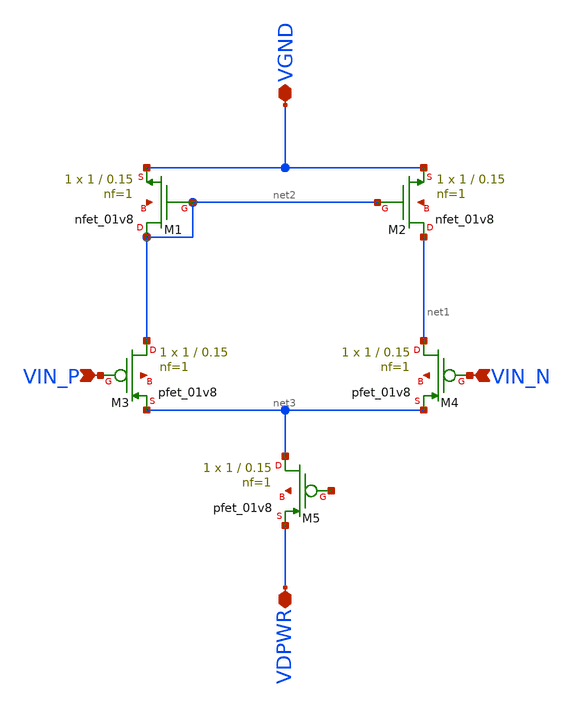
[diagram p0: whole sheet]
** sch_path: xschem/5t_ota.sch
**.subckt 5t_ota VGND VIN_N VIN_P VDPWR
*.iopin VGND
*.ipin VIN_N
*.ipin VIN_P
*.iopin VDPWR
XM1 net2 net2 VGND net4 sky130_fd_pr__nfet_01v8 L=0.15 W=1 nf=1 ad='int((1 + 1)/2) * 1 / 1 * 0.29' as='int((1 + 2)/2) * 1 / 1 * 0.29'
+ pd='2*int((1 + 1)/2) * (1 / 1 + 0.29)' ps='2*int((1 + 2)/2) * (1 / 1 + 0.29)' nrd='0.29 / 1 ' nrs='0.29 / 1 '
+ sa=0 sb=0 sd=0 mult=1 m=1
XM2 net1 net2 VGND net5 sky130_fd_pr__nfet_01v8 L=0.15 W=1 nf=1 ad='int((1 + 1)/2) * 1 / 1 * 0.29' as='int((1 + 2)/2) * 1 / 1 * 0.29'
+ pd='2*int((1 + 1)/2) * (1 / 1 + 0.29)' ps='2*int((1 + 2)/2) * (1 / 1 + 0.29)' nrd='0.29 / 1 ' nrs='0.29 / 1 '
+ sa=0 sb=0 sd=0 mult=1 m=1
XM3 net2 VIN_P net3 net6 sky130_fd_pr__pfet_01v8 L=0.15 W=1 nf=1 ad='int((1 + 1)/2) * 1 / 1 * 0.29' as='int((1 + 2)/2) * 1 / 1 * 0.29'
+ pd='2*int((1 + 1)/2) * (1 / 1 + 0.29)' ps='2*int((1 + 2)/2) * (1 / 1 + 0.29)' nrd='0.29 / 1 ' nrs='0.29 / 1 '
+ sa=0 sb=0 sd=0 mult=1 m=1
XM4 net1 VIN_N net3 net7 sky130_fd_pr__pfet_01v8 L=0.15 W=1 nf=1 ad='int((1 + 1)/2) * 1 / 1 * 0.29' as='int((1 + 2)/2) * 1 / 1 * 0.29'
+ pd='2*int((1 + 1)/2) * (1 / 1 + 0.29)' ps='2*int((1 + 2)/2) * (1 / 1 + 0.29)' nrd='0.29 / 1 ' nrs='0.29 / 1 '
+ sa=0 sb=0 sd=0 mult=1 m=1
XM5 net3 net8 VDPWR net9 sky130_fd_pr__pfet_01v8 L=0.15 W=1 nf=1 ad='int((1 + 1)/2) * 1 / 1 * 0.29' as='int((1 + 2)/2) * 1 / 1 * 0.29'
+ pd='2*int((1 + 1)/2) * (1 / 1 + 0.29)' ps='2*int((1 + 2)/2) * (1 / 1 + 0.29)' nrd='0.29 / 1 ' nrs='0.29 / 1 '
+ sa=0 sb=0 sd=0 mult=1 m=1
**.ends
.end
